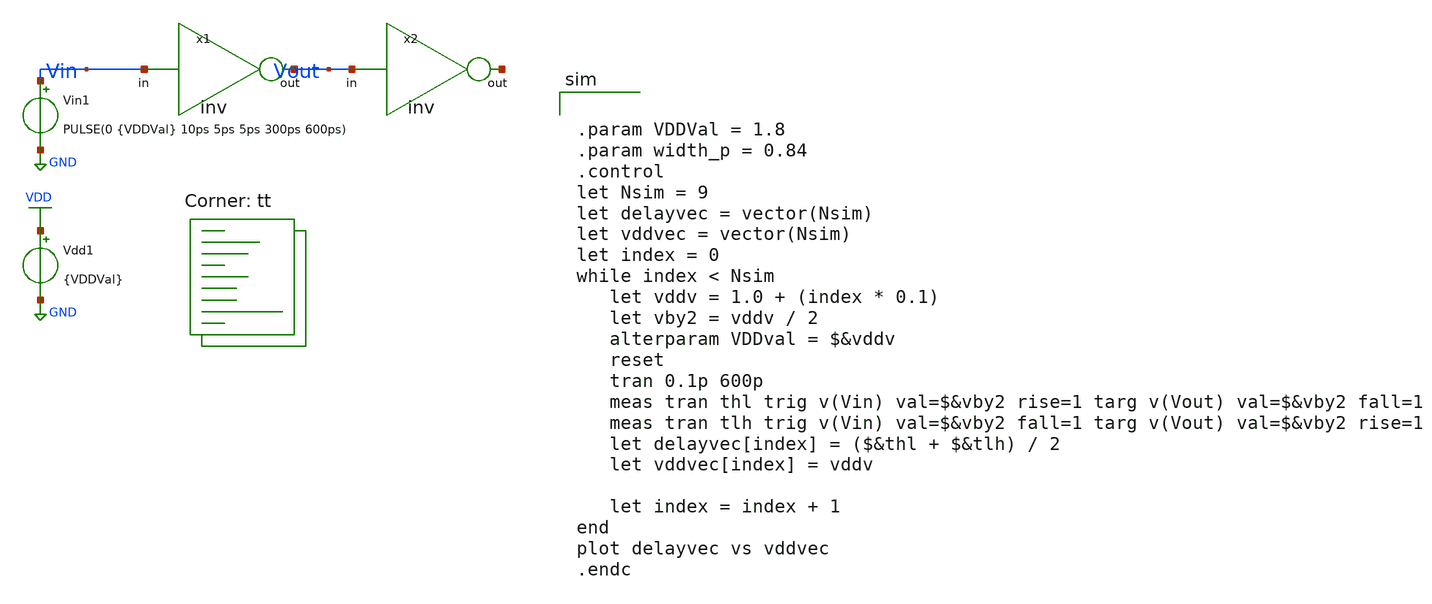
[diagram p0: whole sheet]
** sch_path: tutorial_4/tutorial_4_1b.sch
**.subckt tutorial_4_1b
x1 Vout Vin inv
x2 net1 Vout inv
Vin1 Vin GND PULSE(0 {VDDVal} 10ps 5ps 5ps 300ps 600ps)
Vdd1 VDD GND {VDDVal}
**** begin user architecture code
.lib $::SKYWATER_MODELS/sky130.lib.spice tt


.param VDDVal = 1.8
.param width_p = 0.84
.control
let Nsim = 9
let delayvec = vector(Nsim)
let vddvec = vector(Nsim)
let index = 0
while index < Nsim
   let vddv = 1.0 + (index * 0.1)
   let vby2 = vddv / 2
   alterparam VDDval = $&vddv
   reset
   tran 0.1p 600p
   meas tran thl trig v(Vin) val=$&vby2 rise=1 targ v(Vout) val=$&vby2 fall=1
   meas tran tlh trig v(Vin) val=$&vby2 fall=1 targ v(Vout) val=$&vby2 rise=1
   let delayvec[index] = ($&thl + $&tlh) / 2
   let vddvec[index] = vddv

   let index = index + 1
end
plot delayvec vs vddvec
.endc

**** end user architecture code
**.ends

* expanding   symbol:  /home/EE23B038/ee5311/tutorial_4/inv.sym # of pins=2
** sym_path: tutorial_4/inv.sym
** sch_path: tutorial_4/inv.sch
.subckt inv out in
*.ipin in
*.opin out
XM1 out in GND GND sky130_fd_pr__nfet_01v8 L=0.15 W=0.42 nf=1 ad='int((nf+1)/2) * W/nf * 0.29' as='int((nf+2)/2) * W/nf * 0.29'
+ pd='2*int((nf+1)/2) * (W/nf + 0.29)' ps='2*int((nf+2)/2) * (W/nf + 0.29)' nrd='0.29 / W' nrs='0.29 / W'
+ sa=0 sb=0 sd=0 mult=1 m=1
XM2 out in VDD VDD sky130_fd_pr__pfet_01v8 L=0.15 W={width_p} nf=1 ad='int((nf+1)/2) * W/nf * 0.29' as='int((nf+2)/2) * W/nf * 0.29'
+ pd='2*int((nf+1)/2) * (W/nf + 0.29)' ps='2*int((nf+2)/2) * (W/nf + 0.29)' nrd='0.29 / W' nrs='0.29 / W'
+ sa=0 sb=0 sd=0 mult=1 m=1
.ends

.GLOBAL GND
.GLOBAL VDD
.end
